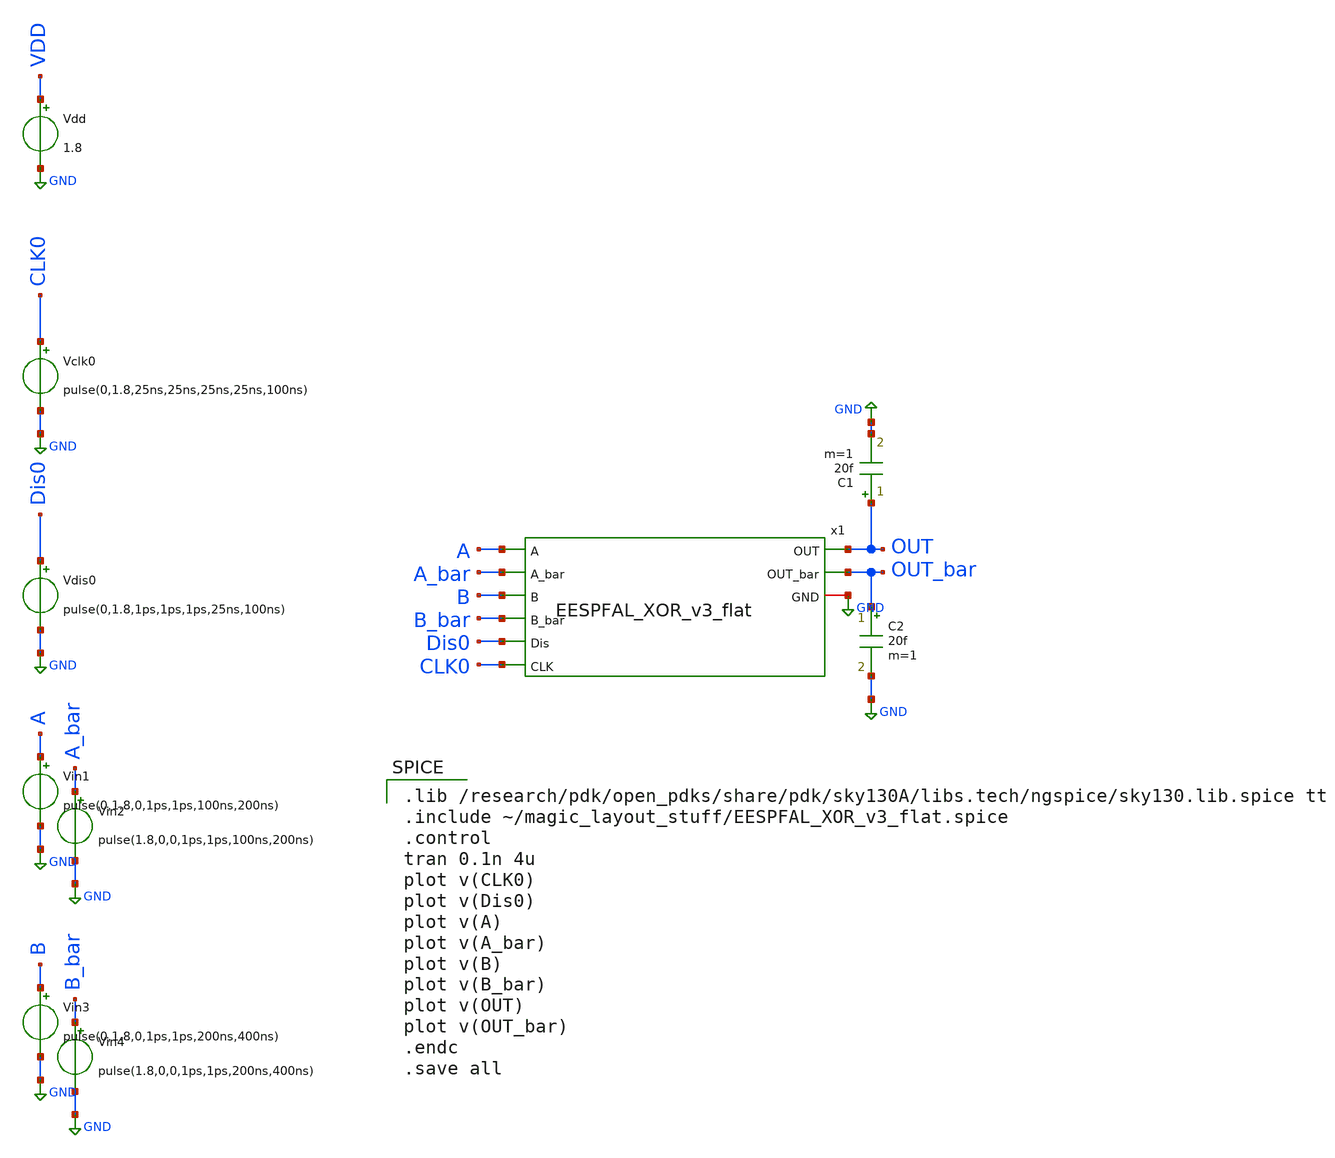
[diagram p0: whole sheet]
** sch_path: skywater_stuff/EESPFAL_XOR_sim.sch
**.subckt EESPFAL_XOR_sim
Vclk0 CLK0 GND pulse(0,1.8,25ns,25ns,25ns,25ns,100ns)
Vin1 A GND pulse(0,1.8,0,1ps,1ps,100ns,200ns)
Vin2 A_bar GND pulse(1.8,0,0,1ps,1ps,100ns,200ns)
Vdis0 Dis0 GND pulse(0,1.8,1ps,1ps,1ps,25ns,100ns)
Vdd VDD GND 1.8
Vin3 B GND pulse(0,1.8,0,1ps,1ps,200ns,400ns)
Vin4 B_bar GND pulse(1.8,0,0,1ps,1ps,200ns,400ns)
x1 OUT A A_bar B B_bar Dis0 OUT_bar GND CLK0 EESPFAL_XOR_v3_flat
C1 OUT GND 20f m=1
C2 OUT_bar GND 20f m=1
**** begin user architecture code

.lib /research/pdk/open_pdks/share/pdk/sky130A/libs.tech/ngspice/sky130.lib.spice tt
.include ~/magic_layout_stuff/EESPFAL_XOR_v3_flat.spice
.control
tran 0.1n 4u
plot v(CLK0)
plot v(Dis0)
plot v(A)
plot v(A_bar)
plot v(B)
plot v(B_bar)
plot v(OUT)
plot v(OUT_bar)
.endc
.save all

**** end user architecture code
**.ends
.GLOBAL GND
.end
